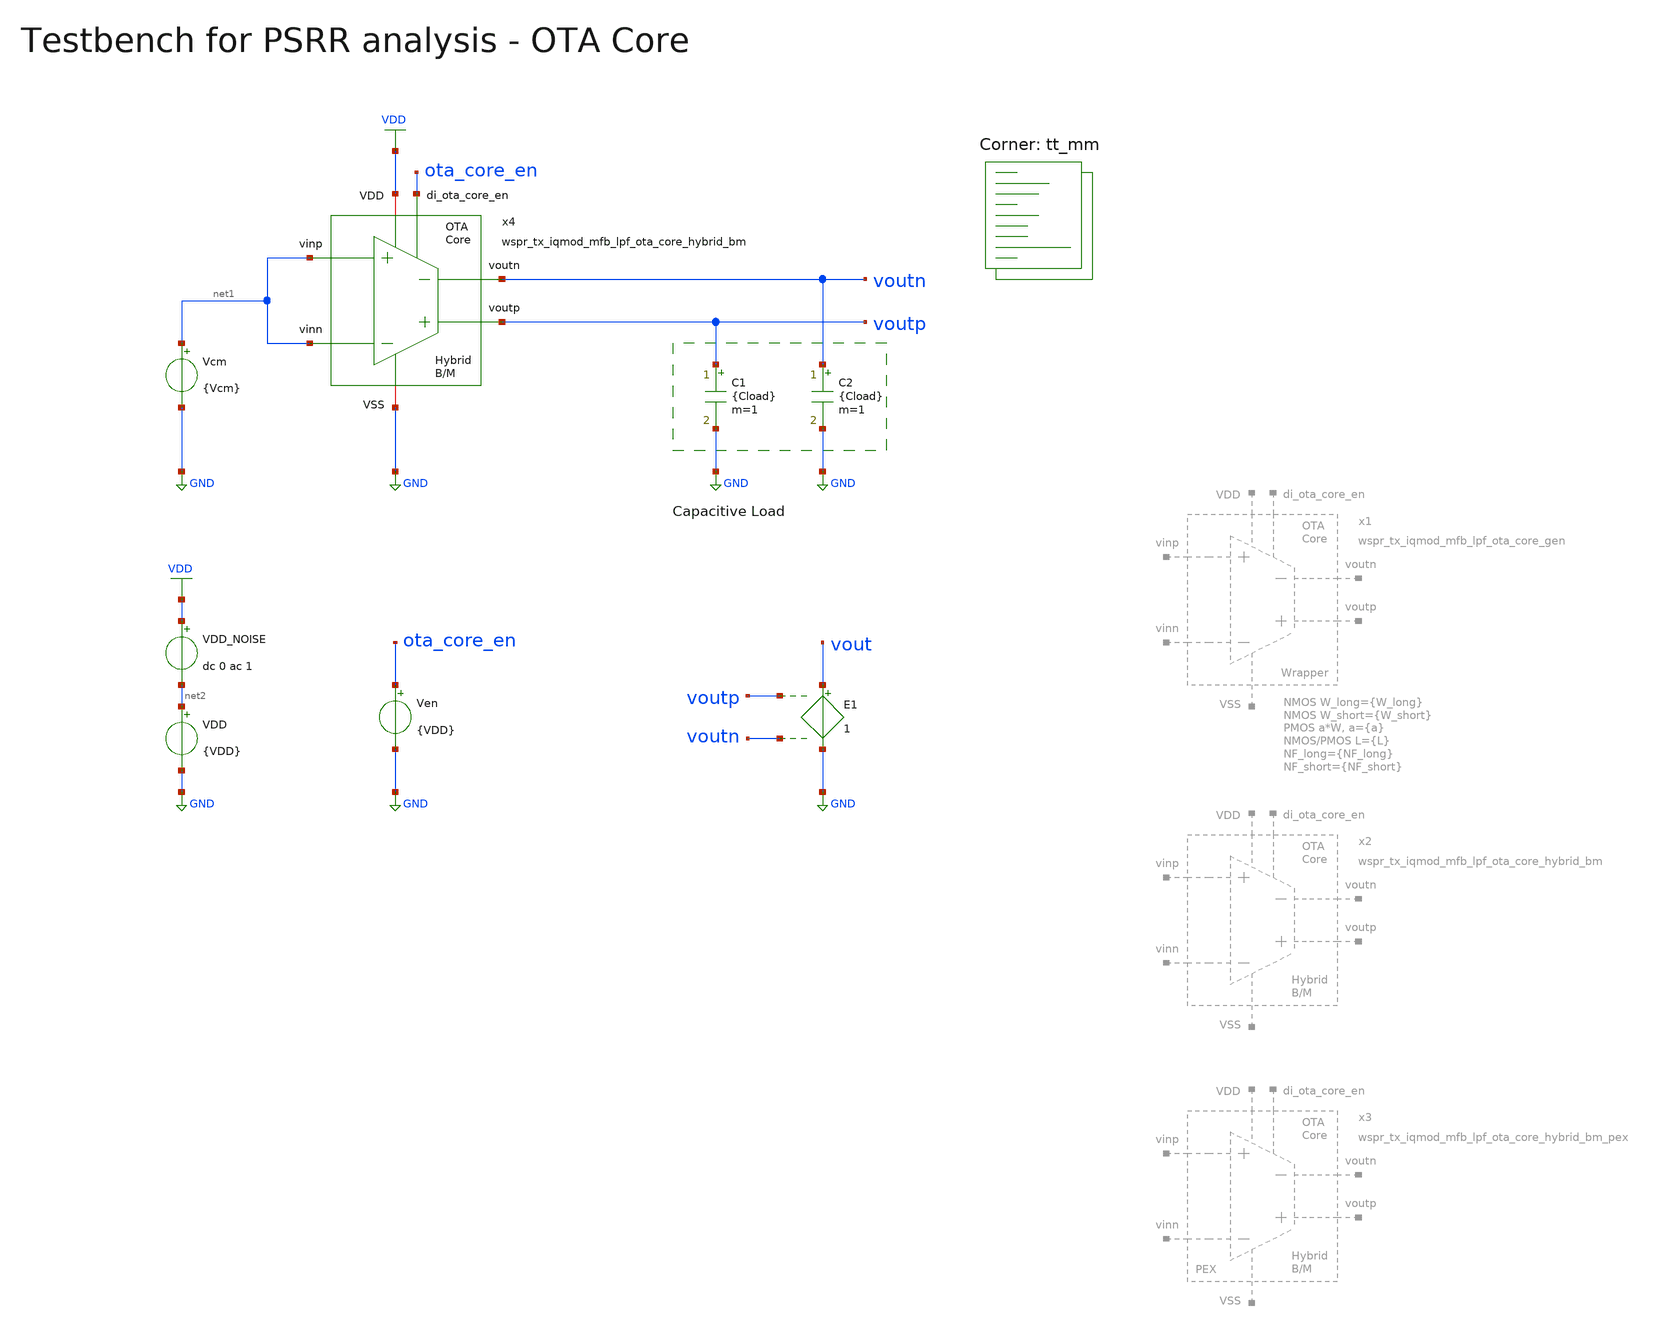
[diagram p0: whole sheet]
** sch_path: sky130/xschem/testbenches/wspr_tx_iqmod_mfb_lpf_ota_core_tb_PSRR.sch
**.subckt wspr_tx_iqmod_mfb_lpf_ota_core_tb_PSRR
C1 voutp GND {Cload} m=1
C2 voutn GND {Cload} m=1
Vcm net1 GND {Vcm}
Ven ota_core_en GND {VDD}
E1 vout GND voutp voutn 1
VDD net2 GND {VDD}
VDD_NOISE VDD net2 dc 0 ac 1
x4 ota_core_en voutp voutn net1 net1 VDD GND wspr_tx_iqmod_mfb_lpf_ota_core_hybrid_bm
**** begin user architecture code


*.include ../../spice/wspr_tx_iqmod_mfb_lpf_ota_core_hybrid_bm_pex.spice
.param VDD=1.8
.param Vcm=VDD/2
.param temp=27
.param Cload=10p
.param W_long=18.0
.param W_short=12.0
.param a=3
.param L=1.0
.param NF_long=6
.param NF_short=4
.options savecurrents klu method=gear reltol=1e-4 abstol=1e-15 gmin=1e-15
.control

* save v(VDD) v(vout) v(voutp) v(voutn)
save all

set wr_vecnames
set wr_singlescale

* User Constants
let f_min = 0.1
let f_max = 1G
let fdc = 1

* Operating Point Analysis
op
remzerovec
write wspr_tx_iqmod_mfb_lpf_ota_core_tb_PSRR.raw
set appendwrite

* AC Analysis
ac dec 101 $&const.f_min $&const.f_max
remzerovec
write wspr_tx_iqmod_mfb_lpf_ota_core_tb_PSRR.raw

* Plotting
let PSRR = v(VDD)/v(vout)
let PSRRp = v(VDD)/v(voutp)
let PSRRn = v(VDD)/v(voutn)

let PSRR_dB = vdb(PSRR)
let PSRRp_dB = vdb(PSRRp)
let PSRRn_dB = vdb(PSRRn)

plot PSRR_dB PSRRp_dB PSRRn_dB ylabel 'PSRR, PSRR+, PSRR-'

* Measurements
meas ac PSRRdc_dB find PSRR_dB when frequency = fdc
print PSRRdc_dB

meas ac PSRRpdc_dB find PSRRp_dB when frequency = fdc
print PSRRpdc_dB

meas ac PSRRndc_dB find PSRRn_dB when frequency = fdc
print PSRRndc_dB

* Write Data
unset appendwrite
set wr_vecnames
set wr_singlescale
wrdata $PROJECT_PATH/python/plot_simulations/data/wspr_tx_iqmod_mfb_lpf_ota_core_tb_PSRR.txt
+ v(PSRR_dB)

*quit
.endc


.lib $::SKYWATER_MODELS/sky130.lib.spice tt_mm
**** end user architecture code
**.ends
.GLOBAL GND
.GLOBAL VDD
.end
